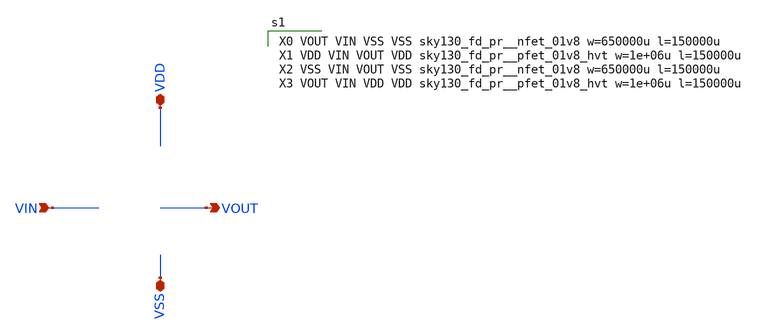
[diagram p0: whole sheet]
** sch_path: inv_2_jm2.sch
**.subckt inv_2_jm2 VIN VOUT VDD VSS
*.ipin VIN
*.opin VOUT
*.iopin VDD
*.iopin VSS
**** begin user architecture code

X0 VOUT VIN VSS VSS sky130_fd_pr__nfet_01v8 w=650000u l=150000u
X1 VDD VIN VOUT VDD sky130_fd_pr__pfet_01v8_hvt w=1e+06u l=150000u
X2 VSS VIN VOUT VSS sky130_fd_pr__nfet_01v8 w=650000u l=150000u
X3 VOUT VIN VDD VDD sky130_fd_pr__pfet_01v8_hvt w=1e+06u l=150000u


**** end user architecture code
**.ends
.end
